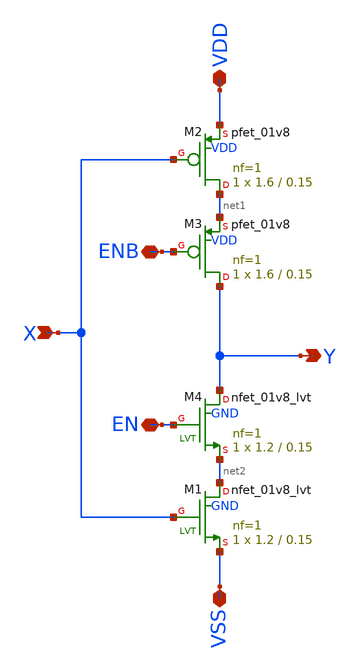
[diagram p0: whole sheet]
** sch_path: schem/tinv.sch
**.subckt tinv X Y VDD VSS EN ENB
*.ipin X
*.opin Y
*.iopin VDD
*.iopin VSS
*.iopin EN
*.iopin ENB
XM1 net2 X VSS GND sky130_fd_pr__nfet_01v8_lvt L=0.15 W=1.2 nf=1 ad='int((nf+1)/2) * W/nf * 0.29' as='int((nf+2)/2) * W/nf * 0.29'
+ pd='2*int((nf+1)/2) * (W/nf + 0.29)' ps='2*int((nf+2)/2) * (W/nf + 0.29)' nrd='0.29 / W' nrs='0.29 / W'
+ sa=0 sb=0 sd=0 mult=1 m=1
XM2 net1 X VDD VDD sky130_fd_pr__pfet_01v8 L=0.15 W=1.6 nf=1 ad='int((nf+1)/2) * W/nf * 0.29' as='int((nf+2)/2) * W/nf * 0.29'
+ pd='2*int((nf+1)/2) * (W/nf + 0.29)' ps='2*int((nf+2)/2) * (W/nf + 0.29)' nrd='0.29 / W' nrs='0.29 / W'
+ sa=0 sb=0 sd=0 mult=1 m=1
XM3 Y ENB net1 VDD sky130_fd_pr__pfet_01v8 L=0.15 W=1.6 nf=1 ad='int((nf+1)/2) * W/nf * 0.29' as='int((nf+2)/2) * W/nf * 0.29'
+ pd='2*int((nf+1)/2) * (W/nf + 0.29)' ps='2*int((nf+2)/2) * (W/nf + 0.29)' nrd='0.29 / W' nrs='0.29 / W'
+ sa=0 sb=0 sd=0 mult=1 m=1
XM4 Y EN net2 GND sky130_fd_pr__nfet_01v8_lvt L=0.15 W=1.2 nf=1 ad='int((nf+1)/2) * W/nf * 0.29' as='int((nf+2)/2) * W/nf * 0.29'
+ pd='2*int((nf+1)/2) * (W/nf + 0.29)' ps='2*int((nf+2)/2) * (W/nf + 0.29)' nrd='0.29 / W' nrs='0.29 / W'
+ sa=0 sb=0 sd=0 mult=1 m=1
**.ends
.end
